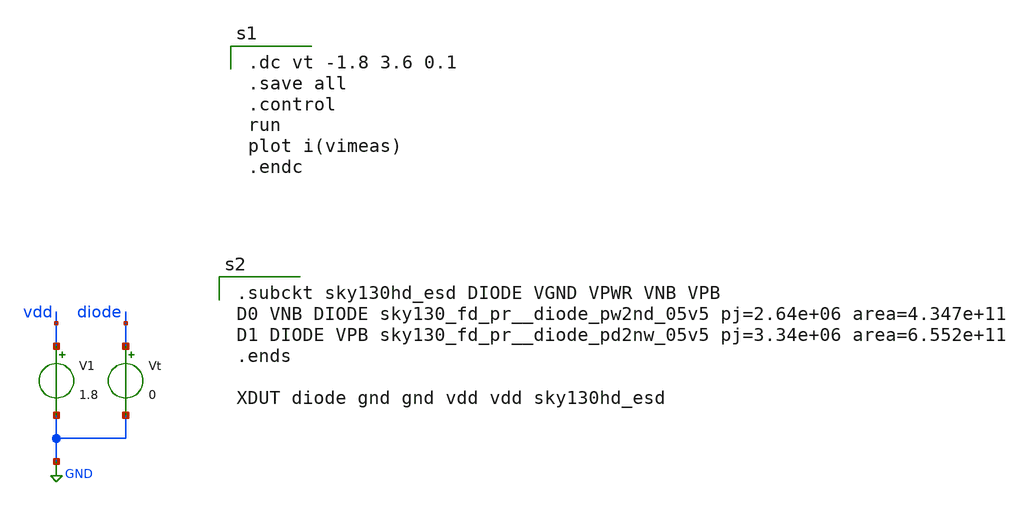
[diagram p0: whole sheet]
** sch_path: xschem/diode_tb.sch
**.subckt diode_tb
V1 vdd GND 1.8
Vt diode GND 0
**** begin user architecture code
.lib $::SKYWATER_MODELS/sky130.lib.spice tt
.include $::PDKPATH/libs.ref/sky130_fd_sc_hs/spice/sky130_fd_sc_hs.spice


.dc vt -1.8 3.6 0.1
.save all
.control
run
plot i(vimeas)
.endc



.subckt sky130hd_esd DIODE VGND VPWR VNB VPB
D0 VNB DIODE sky130_fd_pr__diode_pw2nd_05v5 pj=2.64e+06 area=4.347e+11
D1 DIODE VPB sky130_fd_pr__diode_pd2nw_05v5 pj=3.34e+06 area=6.552e+11
.ends

XDUT diode gnd gnd vdd vdd sky130hd_esd


**** end user architecture code
**.ends
.GLOBAL GND
.end
